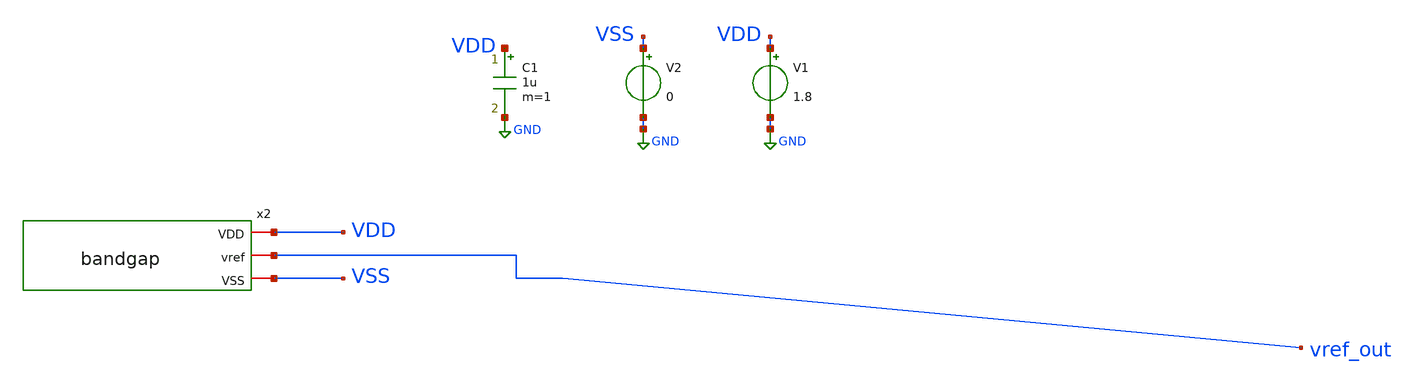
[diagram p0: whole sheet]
** sch_path: xschem/tb_bandgap.sch
**.subckt tb_bandgap
V1 VDD GND 1.8
V2 VSS GND 0
C1 VDD GND 1u m=1
x2 VDD vref_out VSS bandgap
**** begin user architecture code

** opencircuitdesign pdks install
.lib $::SKYWATER_MODELS/sky130.lib.spice tt





*.option  METHOD = GEAR
*.param mc_mm_switch=0
.control
.param mos_mult = 1
.param mos_w = 1
.param mos_l = 0.15
let tempv = 40            ; create a vector vddc and assign 1.8
let vddv = 1.6
repeat 5
 * set temp = $&tempv         ; alter the voltage V1 using vector vddc
alter V1 = $&vddv
  tran 50p 0.5u uic
   let vddv = vddv + 0.1
*  let tempv = tempv + 5   ; update vddc
  write bandgap.raw
  set appendwrite
  reset
end
.endc



**** end user architecture code
**.ends

* expanding   symbol:  bandgap.sym # of pins=3
** sym_path: xschem/bandgap.sym
** sch_path: xschem/bandgap.sch
.subckt bandgap VDD vref VSS
*.iopin VSS
*.iopin VDD
*.iopin vref
XM1 top_gate top_gate VDD VDD sky130_fd_pr__pfet_01v8 L=10 W=10 nf=1 ad='int((nf+1)/2) * W/nf * 0.29'
+ as='int((nf+2)/2) * W/nf * 0.29' pd='2*int((nf+1)/2) * (W/nf + 0.29)' ps='2*int((nf+2)/2) * (W/nf + 0.29)'
+ nrd='0.29 / W' nrs='0.29 / W' sa=0 sb=0 sd=0 mult=1 m=1
XM2 n_gate top_gate VDD VDD sky130_fd_pr__pfet_01v8 L=10 W=10 nf=1 ad='int((nf+1)/2) * W/nf * 0.29' as='int((nf+2)/2) * W/nf * 0.29'
+ pd='2*int((nf+1)/2) * (W/nf + 0.29)' ps='2*int((nf+2)/2) * (W/nf + 0.29)' nrd='0.29 / W' nrs='0.29 / W'
+ sa=0 sb=0 sd=0 mult=1 m=1
XM3 vref top_gate VDD VDD sky130_fd_pr__pfet_01v8 L=10 W=10 nf=1 ad='int((nf+1)/2) * W/nf * 0.29' as='int((nf+2)/2) * W/nf * 0.29'
+ pd='2*int((nf+1)/2) * (W/nf + 0.29)' ps='2*int((nf+2)/2) * (W/nf + 0.29)' nrd='0.29 / W' nrs='0.29 / W'
+ sa=0 sb=0 sd=0 mult=1 m=1
XR4 r4_m6 Va VSS sky130_fd_pr__res_high_po_0p69 L=200 mult=1 m=1
XR1 r1_m8 vref VSS sky130_fd_pr__res_high_po_0p69 L=200 mult=1 m=1
XM9 top_gate n_gate Va VSS sky130_fd_pr__nfet_01v8_lvt L=5 W=10 nf=1 ad='int((nf+1)/2) * W/nf * 0.29'
+ as='int((nf+2)/2) * W/nf * 0.29' pd='2*int((nf+1)/2) * (W/nf + 0.29)' ps='2*int((nf+2)/2) * (W/nf + 0.29)'
+ nrd='0.29 / W' nrs='0.29 / W' sa=0 sb=0 sd=0 mult=1 m=1
XM4 n_gate n_gate Vb VSS sky130_fd_pr__nfet_01v8_lvt L=5 W=10 nf=1 ad='int((nf+1)/2) * W/nf * 0.29' as='int((nf+2)/2) * W/nf * 0.29'
+ pd='2*int((nf+1)/2) * (W/nf + 0.29)' ps='2*int((nf+2)/2) * (W/nf + 0.29)' nrd='0.29 / W' nrs='0.29 / W'
+ sa=0 sb=0 sd=0 mult=1 m=1
XM5 VSS VSS r4_m6 VDD sky130_fd_pr__pfet_01v8_lvt L=5 W=10 nf=1 ad='int((nf+1)/2) * W/nf * 0.29' as='int((nf+2)/2) * W/nf * 0.29'
+ pd='2*int((nf+1)/2) * (W/nf + 0.29)' ps='2*int((nf+2)/2) * (W/nf + 0.29)' nrd='0.29 / W' nrs='0.29 / W'
+ sa=0 sb=0 sd=0 mult=1 m=1
XM6 VSS VSS r1_m8 VDD sky130_fd_pr__pfet_01v8_lvt L=5 W=10 nf=1 ad='int((nf+1)/2) * W/nf * 0.29' as='int((nf+2)/2) * W/nf * 0.29'
+ pd='2*int((nf+1)/2) * (W/nf + 0.29)' ps='2*int((nf+2)/2) * (W/nf + 0.29)' nrd='0.29 / W' nrs='0.29 / W'
+ sa=0 sb=0 sd=0 mult=1 m=1
XM7 VSS VSS Vb VDD sky130_fd_pr__pfet_01v8_lvt L=5 W=3 nf=1 ad='int((nf+1)/2) * W/nf * 0.29' as='int((nf+2)/2) * W/nf * 0.29'
+ pd='2*int((nf+1)/2) * (W/nf + 0.29)' ps='2*int((nf+2)/2) * (W/nf + 0.29)' nrd='0.29 / W' nrs='0.29 / W'
+ sa=0 sb=0 sd=0 mult=1 m=1
.ends

.GLOBAL GND
.end
